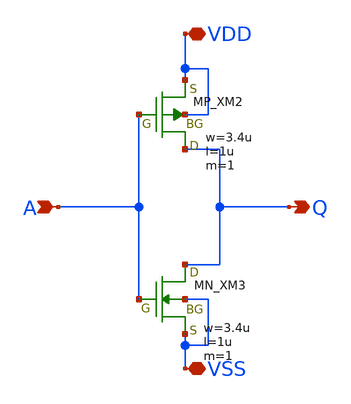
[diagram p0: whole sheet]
** sch_path: member_project/inverter/ZEP/tarry/inverter_tarry.sch
**.subckt inverter_tarry A VSS Q VDD
*.ipin A
*.iopin VSS
*.opin Q
*.iopin VDD
XM2 Q A VDD VDD PMOS w=3.4u l=1u as=0 ad=0 ps=0 pd=0 nrd=0 nrs=0 m=1
XM3 Q A VSS VSS NMOS w=3.4u l=1u as=0 ad=0 ps=0 pd=0 nrd=0 nrs=0 m=1
**.ends
.end
